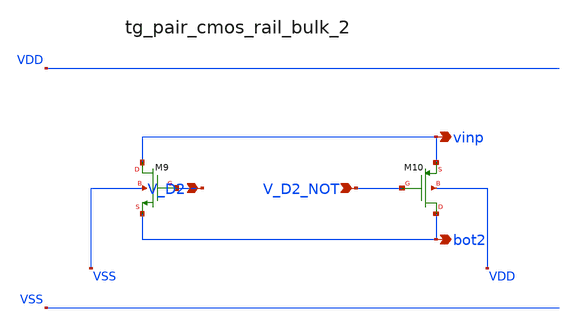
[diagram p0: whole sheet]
** sch_path: analog-db/raw/sw_003_binary_capbank/hier/blocks/tg_pair_cmos_rail_bulk_2.sch
**.subckt tg_pair_cmos_rail_bulk_2 V_D2 V_D2_NOT vinp bot2
*.ipin V_D2
*.ipin V_D2_NOT
*.opin vinp
*.opin bot2
XM10 bot2 V_D2_NOT vinp VDD sg13_lv_pmos w=x_dut_xm10_w l=x_dut_xm10_l ng=1 m=x_dut_xm10_m
XM9 vinp V_D2 bot2 VSS sg13_lv_nmos w=x_dut_xm9_w l=x_dut_xm9_l ng=1 m=x_dut_xm9_m
**.ends
.end
